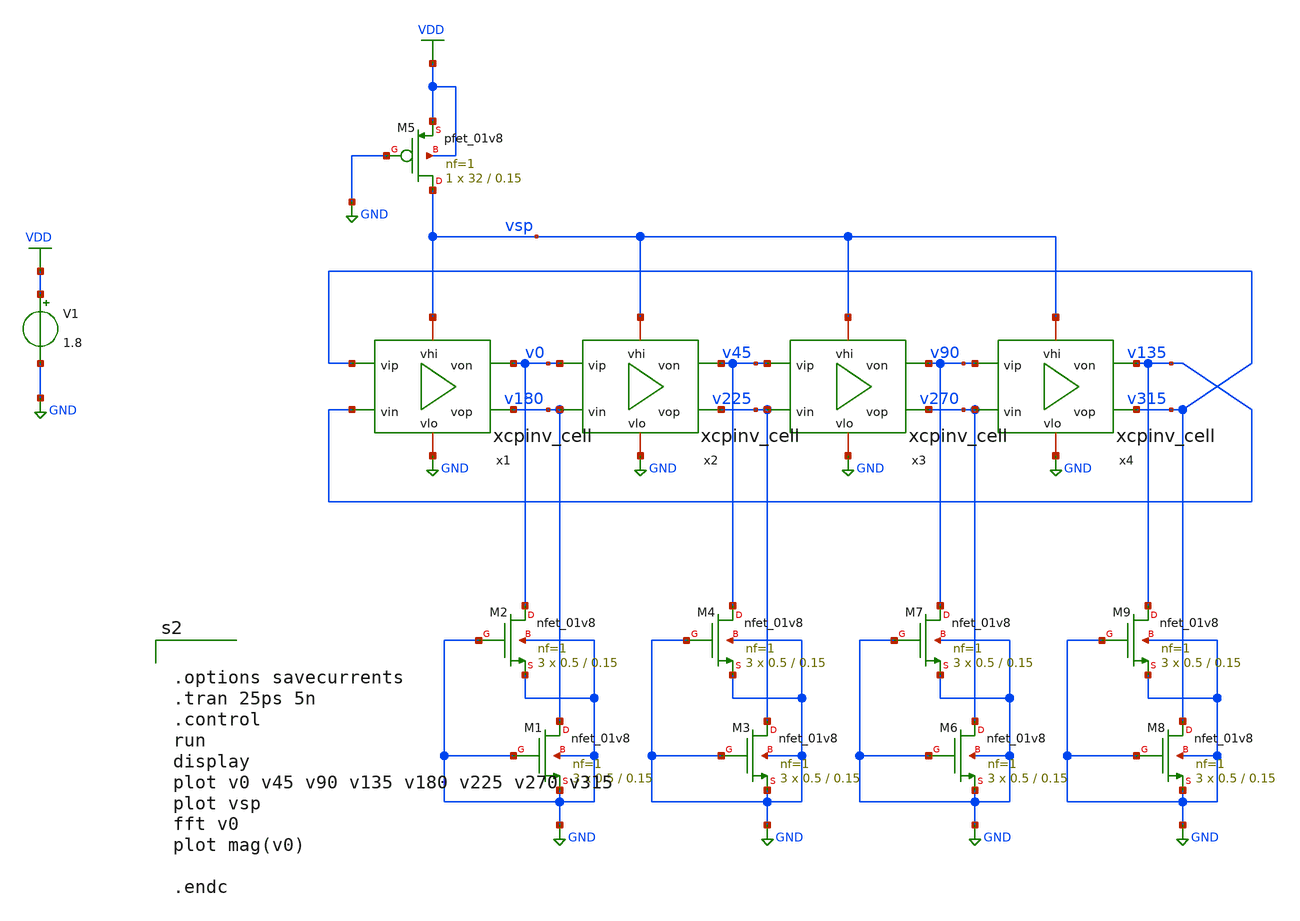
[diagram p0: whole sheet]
** sch_path: xschem/xcp_osc_tb.sch
**.subckt xcp_osc_tb
V1 VDD GND 1.8
x1 vsp v315 v135 GND v180 v0 xcpinv_cell
x2 vsp v0 v180 GND v225 v45 xcpinv_cell
XM1 v180 GND GND GND sky130_fd_pr__nfet_01v8 L=0.15 W=0.5 nf=1 ad='int((nf+1)/2) * W/nf * 0.29' as='int((nf+2)/2) * W/nf * 0.29'
+ pd='2*int((nf+1)/2) * (W/nf + 0.29)' ps='2*int((nf+2)/2) * (W/nf + 0.29)' nrd='0.29 / W' nrs='0.29 / W'
+ sa=0 sb=0 sd=0 mult=3 m=3
XM2 v0 GND GND GND sky130_fd_pr__nfet_01v8 L=0.15 W=0.5 nf=1 ad='int((nf+1)/2) * W/nf * 0.29' as='int((nf+2)/2) * W/nf * 0.29'
+ pd='2*int((nf+1)/2) * (W/nf + 0.29)' ps='2*int((nf+2)/2) * (W/nf + 0.29)' nrd='0.29 / W' nrs='0.29 / W'
+ sa=0 sb=0 sd=0 mult=3 m=3
XM3 v225 GND GND GND sky130_fd_pr__nfet_01v8 L=0.15 W=0.5 nf=1 ad='int((nf+1)/2) * W/nf * 0.29' as='int((nf+2)/2) * W/nf * 0.29'
+ pd='2*int((nf+1)/2) * (W/nf + 0.29)' ps='2*int((nf+2)/2) * (W/nf + 0.29)' nrd='0.29 / W' nrs='0.29 / W'
+ sa=0 sb=0 sd=0 mult=3 m=3
XM4 v45 GND GND GND sky130_fd_pr__nfet_01v8 L=0.15 W=0.5 nf=1 ad='int((nf+1)/2) * W/nf * 0.29' as='int((nf+2)/2) * W/nf * 0.29'
+ pd='2*int((nf+1)/2) * (W/nf + 0.29)' ps='2*int((nf+2)/2) * (W/nf + 0.29)' nrd='0.29 / W' nrs='0.29 / W'
+ sa=0 sb=0 sd=0 mult=3 m=3
XM5 vsp GND VDD VDD sky130_fd_pr__pfet_01v8 L=0.15 W=32 nf=1 ad='int((nf+1)/2) * W/nf * 0.29' as='int((nf+2)/2) * W/nf * 0.29'
+ pd='2*int((nf+1)/2) * (W/nf + 0.29)' ps='2*int((nf+2)/2) * (W/nf + 0.29)' nrd='0.29 / W' nrs='0.29 / W'
+ sa=0 sb=0 sd=0 mult=1 m=1
x3 vsp v45 v225 GND v270 v90 xcpinv_cell
XM6 v270 GND GND GND sky130_fd_pr__nfet_01v8 L=0.15 W=0.5 nf=1 ad='int((nf+1)/2) * W/nf * 0.29' as='int((nf+2)/2) * W/nf * 0.29'
+ pd='2*int((nf+1)/2) * (W/nf + 0.29)' ps='2*int((nf+2)/2) * (W/nf + 0.29)' nrd='0.29 / W' nrs='0.29 / W'
+ sa=0 sb=0 sd=0 mult=3 m=3
XM7 v90 GND GND GND sky130_fd_pr__nfet_01v8 L=0.15 W=0.5 nf=1 ad='int((nf+1)/2) * W/nf * 0.29' as='int((nf+2)/2) * W/nf * 0.29'
+ pd='2*int((nf+1)/2) * (W/nf + 0.29)' ps='2*int((nf+2)/2) * (W/nf + 0.29)' nrd='0.29 / W' nrs='0.29 / W'
+ sa=0 sb=0 sd=0 mult=3 m=3
x4 vsp v90 v270 GND v315 v135 xcpinv_cell
XM8 v315 GND GND GND sky130_fd_pr__nfet_01v8 L=0.15 W=0.5 nf=1 ad='int((nf+1)/2) * W/nf * 0.29' as='int((nf+2)/2) * W/nf * 0.29'
+ pd='2*int((nf+1)/2) * (W/nf + 0.29)' ps='2*int((nf+2)/2) * (W/nf + 0.29)' nrd='0.29 / W' nrs='0.29 / W'
+ sa=0 sb=0 sd=0 mult=3 m=3
XM9 v135 GND GND GND sky130_fd_pr__nfet_01v8 L=0.15 W=0.5 nf=1 ad='int((nf+1)/2) * W/nf * 0.29' as='int((nf+2)/2) * W/nf * 0.29'
+ pd='2*int((nf+1)/2) * (W/nf + 0.29)' ps='2*int((nf+2)/2) * (W/nf + 0.29)' nrd='0.29 / W' nrs='0.29 / W'
+ sa=0 sb=0 sd=0 mult=3 m=3
**** begin user architecture code
.lib $::SKYWATER_MODELS/sky130.lib.spice tt
* .include $::PDKPATH/libs.ref/sky130_fd_sc_hvl/spice/sky130_fd_sc_hvl.spice



.options savecurrents
.tran 25ps 5n
.control
run
display
plot v0 v45 v90 v135 v180 v225 v270 v315
plot vsp
fft v0
plot mag(v0)

.endc


**** end user architecture code
**.ends

* expanding   symbol:  xcpinv_cell.sym # of pins=6
** sym_path: xschem/xcpinv_cell.sym
** sch_path: xschem/xcpinv_cell.sch
.subckt xcpinv_cell vhi vip vin vlo vop von
*.iopin vhi
*.iopin vlo
*.ipin vip
*.ipin vin
*.opin von
*.opin vop
XM1 von vip vhi vhi sky130_fd_pr__pfet_01v8 L=0.15 W=16 nf=1 ad='int((nf+1)/2) * W/nf * 0.29' as='int((nf+2)/2) * W/nf * 0.29'
+ pd='2*int((nf+1)/2) * (W/nf + 0.29)' ps='2*int((nf+2)/2) * (W/nf + 0.29)' nrd='0.29 / W' nrs='0.29 / W'
+ sa=0 sb=0 sd=0 mult=1 m=1
XM2 von vip vlo vlo sky130_fd_pr__nfet_01v8 L=0.15 W=8 nf=1 ad='int((nf+1)/2) * W/nf * 0.29' as='int((nf+2)/2) * W/nf * 0.29'
+ pd='2*int((nf+1)/2) * (W/nf + 0.29)' ps='2*int((nf+2)/2) * (W/nf + 0.29)' nrd='0.29 / W' nrs='0.29 / W'
+ sa=0 sb=0 sd=0 mult=1 m=1
XM3 von vop vhi vhi sky130_fd_pr__pfet_01v8 L=0.15 W=8 nf=1 ad='int((nf+1)/2) * W/nf * 0.29' as='int((nf+2)/2) * W/nf * 0.29'
+ pd='2*int((nf+1)/2) * (W/nf + 0.29)' ps='2*int((nf+2)/2) * (W/nf + 0.29)' nrd='0.29 / W' nrs='0.29 / W'
+ sa=0 sb=0 sd=0 mult=1 m=1
XM4 von vop vlo vlo sky130_fd_pr__nfet_01v8 L=0.15 W=4 nf=1 ad='int((nf+1)/2) * W/nf * 0.29' as='int((nf+2)/2) * W/nf * 0.29'
+ pd='2*int((nf+1)/2) * (W/nf + 0.29)' ps='2*int((nf+2)/2) * (W/nf + 0.29)' nrd='0.29 / W' nrs='0.29 / W'
+ sa=0 sb=0 sd=0 mult=1 m=1
XM5 vop von vhi vhi sky130_fd_pr__pfet_01v8 L=0.15 W=8 nf=1 ad='int((nf+1)/2) * W/nf * 0.29' as='int((nf+2)/2) * W/nf * 0.29'
+ pd='2*int((nf+1)/2) * (W/nf + 0.29)' ps='2*int((nf+2)/2) * (W/nf + 0.29)' nrd='0.29 / W' nrs='0.29 / W'
+ sa=0 sb=0 sd=0 mult=1 m=1
XM6 vop von vlo vlo sky130_fd_pr__nfet_01v8 L=0.15 W=4 nf=1 ad='int((nf+1)/2) * W/nf * 0.29' as='int((nf+2)/2) * W/nf * 0.29'
+ pd='2*int((nf+1)/2) * (W/nf + 0.29)' ps='2*int((nf+2)/2) * (W/nf + 0.29)' nrd='0.29 / W' nrs='0.29 / W'
+ sa=0 sb=0 sd=0 mult=1 m=1
XM7 vop vin vhi vhi sky130_fd_pr__pfet_01v8 L=0.15 W=16 nf=1 ad='int((nf+1)/2) * W/nf * 0.29' as='int((nf+2)/2) * W/nf * 0.29'
+ pd='2*int((nf+1)/2) * (W/nf + 0.29)' ps='2*int((nf+2)/2) * (W/nf + 0.29)' nrd='0.29 / W' nrs='0.29 / W'
+ sa=0 sb=0 sd=0 mult=1 m=1
XM8 vop vin vlo vlo sky130_fd_pr__nfet_01v8 L=0.15 W=8 nf=1 ad='int((nf+1)/2) * W/nf * 0.29' as='int((nf+2)/2) * W/nf * 0.29'
+ pd='2*int((nf+1)/2) * (W/nf + 0.29)' ps='2*int((nf+2)/2) * (W/nf + 0.29)' nrd='0.29 / W' nrs='0.29 / W'
+ sa=0 sb=0 sd=0 mult=1 m=1
.ends

.GLOBAL VDD
.GLOBAL GND
.end
